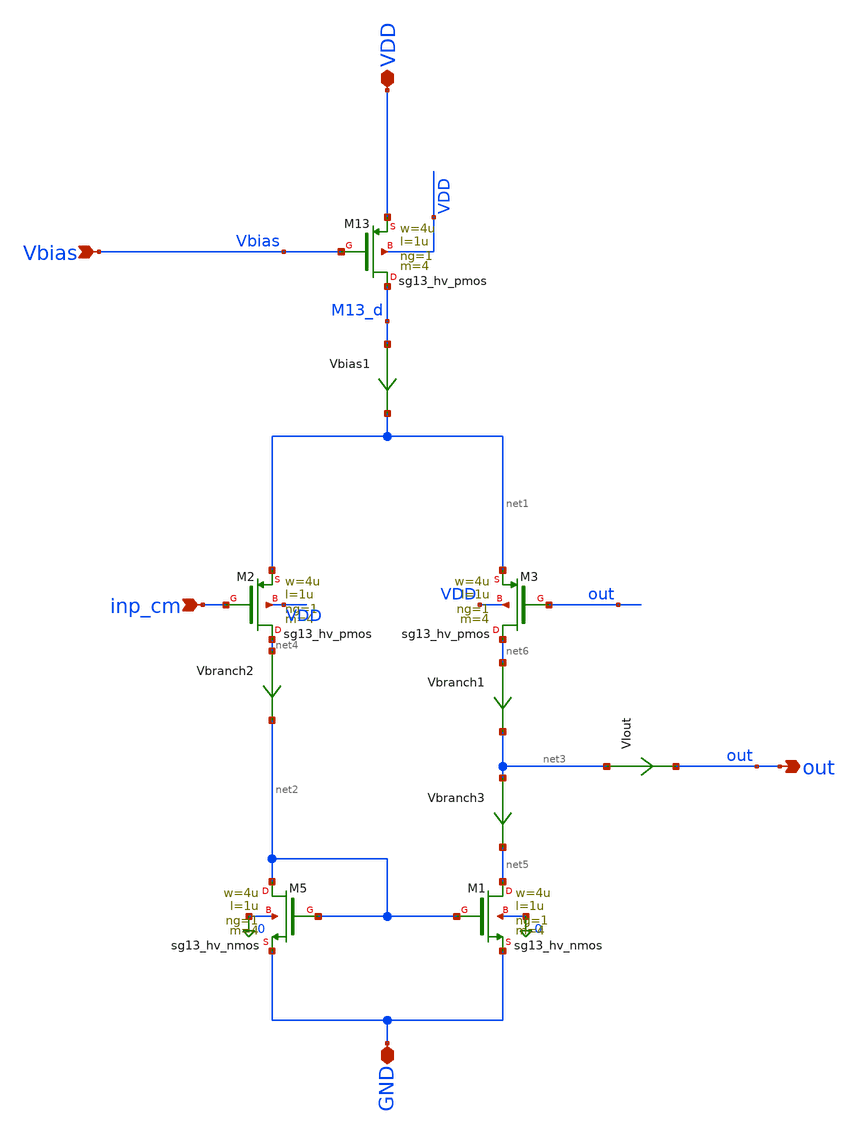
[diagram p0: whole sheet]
** sch_path: xschem/buffer_final.sch
**.subckt buffer_final inp_cm out VDD GND Vbias
*.ipin inp_cm
*.opin out
*.iopin VDD
*.iopin GND
*.ipin Vbias
VIout net3 out 0
.save i(viout)
XM2 net4 inp_cm net1 VDD sg13_hv_pmos w=4u l=1u ng=1 m=4 mm_ok=1
XM5 net2 net2 GND 0 sg13_hv_nmos w=4u l=1u ng=1 m=4 mm_ok=1
Vbias1 M13_d net1 0
.save i(vbias1)
Vbranch1 net6 net3 0
.save i(vbranch1)
Vbranch2 net4 net2 0
.save i(vbranch2)
Vbranch3 net3 net5 0
.save i(vbranch3)
XM13 M13_d Vbias VDD VDD sg13_hv_pmos w=4u l=1u ng=1 m=4 mm_ok=1
XM3 net6 out net1 VDD sg13_hv_pmos w=4u l=1u ng=1 m=4 mm_ok=1
XM1 net5 net2 GND 0 sg13_hv_nmos w=4u l=1u ng=1 m=4 mm_ok=1
**.ends
.end
